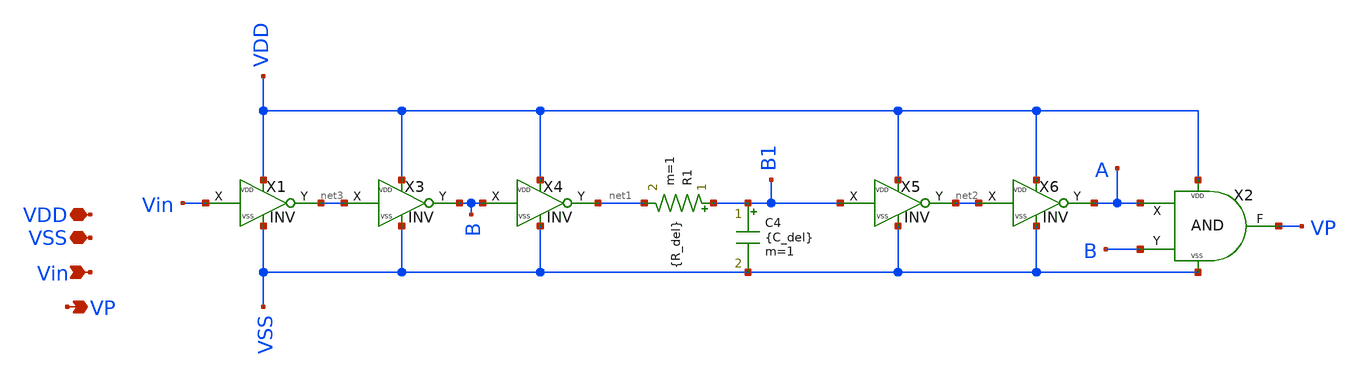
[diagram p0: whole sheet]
** sch_path: xschem/SPG/SPG.sch
**.subckt SPG VDD Vin VP VSS
*.iopin VDD
*.ipin Vin
*.opin VP
*.iopin VSS
R1 B1 net1 {R_del} m=1
C4 B1 VSS {C_del} m=1
X1 Vin net3 VDD VSS INV
X2 A B VSS VDD VP AND
X3 net3 B VDD VSS INV
X4 B net1 VDD VSS INV
X5 B1 net2 VDD VSS INV
X6 net2 A VDD VSS INV
**** begin user architecture code



**** end user architecture code
**.ends

* expanding   symbol:  ../DigitalGates/INV.sym # of pins=4
** sym_path: xschem/DigitalGates/INV.sym
** sch_path: xschem/DigitalGates/INV.sch
.subckt INV X Y VDD VSS
*.iopin VDD
*.ipin X
*.opin Y
*.iopin VSS
XM3 Y X VSS VSS sg13_lv_nmos w={w_inv} l={l_inv} ng=1 m={mult} mm_ok=1
XM4 Y X VDD VDD sg13_lv_pmos w={w_inv} l={l_inv} ng=1 m={mult*3} mm_ok=1
**** begin user architecture code



**** end user architecture code
.ends


* expanding   symbol:  ../DigitalGates/AND.sym # of pins=5
** sym_path: xschem/DigitalGates/AND.sym
** sch_path: xschem/DigitalGates/AND.sch
.subckt AND X Y VSS VDD F
*.iopin VDD
*.ipin X
*.opin F
*.iopin VSS
*.ipin Y
XM1 net1 X net2 VSS sg13_lv_nmos w={w_N_AND} l={l_N_AND} ng=1 m={mult} mm_ok=1
XM2 F net1 VDD VDD sg13_lv_pmos w={w_P_AND} l={l_P_AND} ng=1 m={mult*3} mm_ok=1
XM3 net2 Y VSS VSS sg13_lv_nmos w={w_N_AND} l={l_N_AND} ng=1 m={mult} mm_ok=1
XM4 F net1 VSS VSS sg13_lv_nmos w={w_N_AND} l={l_N_AND} ng=1 m={mult} mm_ok=1
XM5 net1 Y VDD VDD sg13_lv_pmos w={w_P_AND} l={l_P_AND} ng=1 m={mult*3} mm_ok=1
XM6 net1 X VDD VDD sg13_lv_pmos w={w_P_AND} l={l_P_AND} ng=1 m={mult*3} mm_ok=1
**** begin user architecture code



**** end user architecture code
.ends

.end
